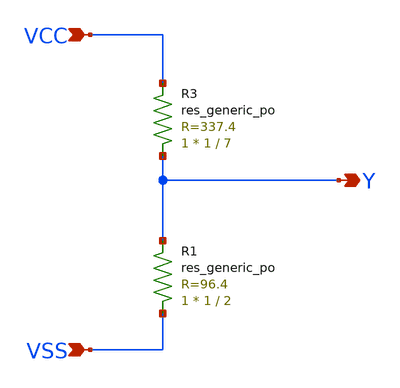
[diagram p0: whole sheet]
** sch_path: xschem/vDivider_04.sch
**.subckt vDivider_04 VCC VSS Y
*.ipin VCC
*.ipin VSS
*.opin Y
XR3 Y VCC sky130_fd_pr__res_generic_po W=1 L=7 m=1
XR1 VSS Y sky130_fd_pr__res_generic_po W=1 L=2 m=1
**.ends
.end
